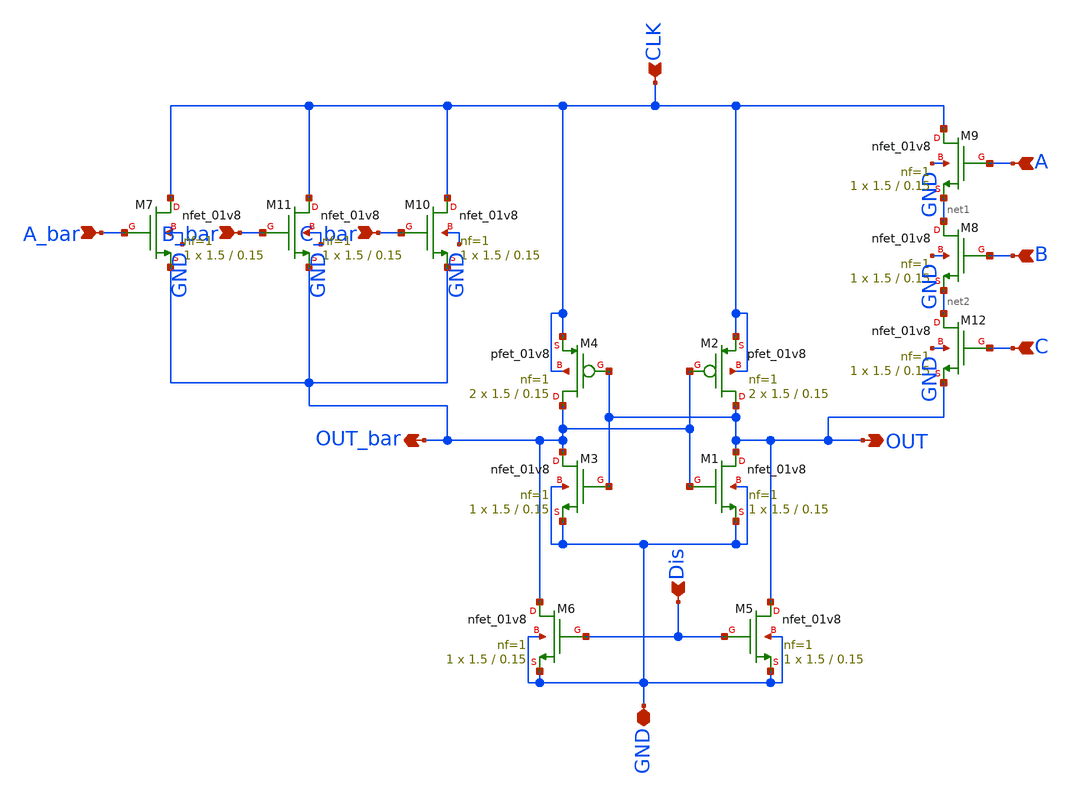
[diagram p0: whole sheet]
** sch_path: skywater_stuff/EESPFAL_3in_NAND_v2.sch
**.subckt EESPFAL_3in_NAND_v2 A A_bar B B_bar C C_bar OUT OUT_bar Dis GND CLK
*.ipin A
*.ipin A_bar
*.ipin B
*.ipin B_bar
*.ipin C
*.ipin C_bar
*.opin OUT
*.opin OUT_bar
*.ipin Dis
*.iopin GND
*.ipin CLK
XM4 OUT_bar OUT CLK CLK sky130_fd_pr__pfet_01v8 L=0.15 W=1.5 nf=1 ad='int((nf+1)/2) * W/nf * 0.29' as='int((nf+2)/2) * W/nf * 0.29'
+ pd='2*int((nf+1)/2) * (W/nf + 0.29)' ps='2*int((nf+2)/2) * (W/nf + 0.29)' nrd='0.29 / W' nrs='0.29 / W'
+ sa=0 sb=0 sd=0 mult=2 m=2
XM3 OUT_bar OUT GND GND sky130_fd_pr__nfet_01v8 L=0.15 W=1.5 nf=1 ad='int((nf+1)/2) * W/nf * 0.29' as='int((nf+2)/2) * W/nf * 0.29'
+ pd='2*int((nf+1)/2) * (W/nf + 0.29)' ps='2*int((nf+2)/2) * (W/nf + 0.29)' nrd='0.29 / W' nrs='0.29 / W'
+ sa=0 sb=0 sd=0 mult=1 m=1
XM2 OUT OUT_bar CLK CLK sky130_fd_pr__pfet_01v8 L=0.15 W=1.5 nf=1 ad='int((nf+1)/2) * W/nf * 0.29' as='int((nf+2)/2) * W/nf * 0.29'
+ pd='2*int((nf+1)/2) * (W/nf + 0.29)' ps='2*int((nf+2)/2) * (W/nf + 0.29)' nrd='0.29 / W' nrs='0.29 / W'
+ sa=0 sb=0 sd=0 mult=2 m=2
XM11 CLK B_bar OUT_bar GND sky130_fd_pr__nfet_01v8 L=0.15 W=1.5 nf=1 ad='int((nf+1)/2) * W/nf * 0.29'
+ as='int((nf+2)/2) * W/nf * 0.29' pd='2*int((nf+1)/2) * (W/nf + 0.29)' ps='2*int((nf+2)/2) * (W/nf + 0.29)'
+ nrd='0.29 / W' nrs='0.29 / W' sa=0 sb=0 sd=0 mult=1 m=1
XM7 CLK A_bar OUT_bar GND sky130_fd_pr__nfet_01v8 L=0.15 W=1.5 nf=1 ad='int((nf+1)/2) * W/nf * 0.29'
+ as='int((nf+2)/2) * W/nf * 0.29' pd='2*int((nf+1)/2) * (W/nf + 0.29)' ps='2*int((nf+2)/2) * (W/nf + 0.29)'
+ nrd='0.29 / W' nrs='0.29 / W' sa=0 sb=0 sd=0 mult=1 m=1
XM8 net1 B net2 GND sky130_fd_pr__nfet_01v8 L=0.15 W=1.5 nf=1 ad='int((nf+1)/2) * W/nf * 0.29' as='int((nf+2)/2) * W/nf * 0.29'
+ pd='2*int((nf+1)/2) * (W/nf + 0.29)' ps='2*int((nf+2)/2) * (W/nf + 0.29)' nrd='0.29 / W' nrs='0.29 / W'
+ sa=0 sb=0 sd=0 mult=1 m=1
XM1 OUT OUT_bar GND GND sky130_fd_pr__nfet_01v8 L=0.15 W=1.5 nf=1 ad='int((nf+1)/2) * W/nf * 0.29' as='int((nf+2)/2) * W/nf * 0.29'
+ pd='2*int((nf+1)/2) * (W/nf + 0.29)' ps='2*int((nf+2)/2) * (W/nf + 0.29)' nrd='0.29 / W' nrs='0.29 / W'
+ sa=0 sb=0 sd=0 mult=1 m=1
XM5 OUT Dis GND GND sky130_fd_pr__nfet_01v8 L=0.15 W=1.5 nf=1 ad='int((nf+1)/2) * W/nf * 0.29' as='int((nf+2)/2) * W/nf * 0.29'
+ pd='2*int((nf+1)/2) * (W/nf + 0.29)' ps='2*int((nf+2)/2) * (W/nf + 0.29)' nrd='0.29 / W' nrs='0.29 / W'
+ sa=0 sb=0 sd=0 mult=1 m=1
XM6 OUT_bar Dis GND GND sky130_fd_pr__nfet_01v8 L=0.15 W=1.5 nf=1 ad='int((nf+1)/2) * W/nf * 0.29' as='int((nf+2)/2) * W/nf * 0.29'
+ pd='2*int((nf+1)/2) * (W/nf + 0.29)' ps='2*int((nf+2)/2) * (W/nf + 0.29)' nrd='0.29 / W' nrs='0.29 / W'
+ sa=0 sb=0 sd=0 mult=1 m=1
XM10 CLK C_bar OUT_bar GND sky130_fd_pr__nfet_01v8 L=0.15 W=1.5 nf=1 ad='int((nf+1)/2) * W/nf * 0.29'
+ as='int((nf+2)/2) * W/nf * 0.29' pd='2*int((nf+1)/2) * (W/nf + 0.29)' ps='2*int((nf+2)/2) * (W/nf + 0.29)'
+ nrd='0.29 / W' nrs='0.29 / W' sa=0 sb=0 sd=0 mult=1 m=1
XM9 CLK A net1 GND sky130_fd_pr__nfet_01v8 L=0.15 W=1.5 nf=1 ad='int((nf+1)/2) * W/nf * 0.29' as='int((nf+2)/2) * W/nf * 0.29'
+ pd='2*int((nf+1)/2) * (W/nf + 0.29)' ps='2*int((nf+2)/2) * (W/nf + 0.29)' nrd='0.29 / W' nrs='0.29 / W'
+ sa=0 sb=0 sd=0 mult=1 m=1
XM12 net2 C OUT GND sky130_fd_pr__nfet_01v8 L=0.15 W=1.5 nf=1 ad='int((nf+1)/2) * W/nf * 0.29' as='int((nf+2)/2) * W/nf * 0.29'
+ pd='2*int((nf+1)/2) * (W/nf + 0.29)' ps='2*int((nf+2)/2) * (W/nf + 0.29)' nrd='0.29 / W' nrs='0.29 / W'
+ sa=0 sb=0 sd=0 mult=1 m=1
**.ends
.end
